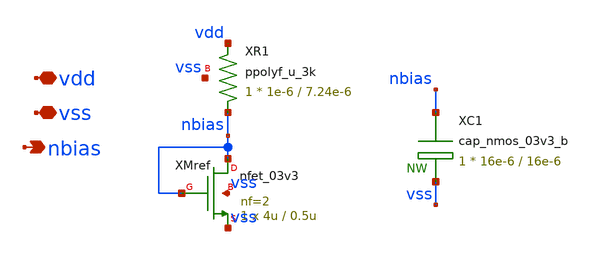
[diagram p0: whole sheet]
** sch_path: blocks/adc/comp-array/bias.sch
**.subckt bias vdd vss nbias
*.iopin vdd
*.iopin vss
*.opin nbias
XMref nbias nbias vss vss nfet_03v3 L=0.5u W=4u nf=2 ad='int((nf+1)/2) * W/nf * 0.18u' as='int((nf+2)/2) * W/nf * 0.18u'
+ pd='2*int((nf+1)/2) * (W/nf + 0.18u)' ps='2*int((nf+2)/2) * (W/nf + 0.18u)' nrd='0.18u / W' nrs='0.18u / W'
+ sa=0 sb=0 sd=0 m=1
XR1 nbias vdd vss ppolyf_u_3k r_width=1e-6 r_length=7.24e-6 m=1
XC1 nbias vss cap_nmos_03v3_b c_width=16e-6 c_length=16e-6 m=1
**.ends
.end
